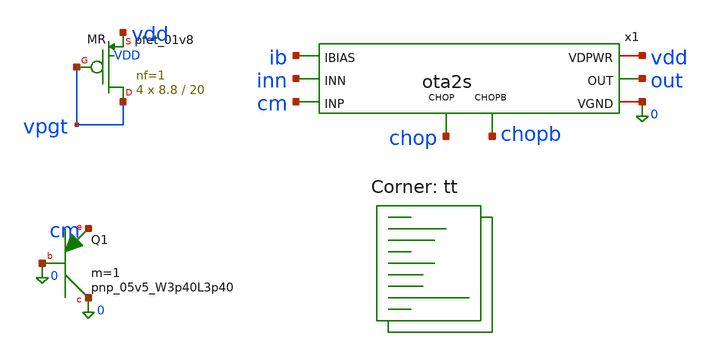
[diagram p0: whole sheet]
** sch_path: xschem/tb_m3_sens.sch
**.subckt tb_m3_sens
x1 cm inn out vdd 0 ib chop chopb ota2s
XMR vpgt vpgt vdd VDD sky130_fd_pr__pfet_01v8 L=20 W=8.8 nf=1 ad='int((1 + 1)/2) * 8.8 / 1 * 0.29' as='int((1 + 2)/2) * 8.8 / 1 * 0.29'
+ pd='2*int((1 + 1)/2) * (8.8 / 1 + 0.29)' ps='2*int((1 + 2)/2) * (8.8 / 1 + 0.29)' nrd='0.29 / 8.8 ' nrs='0.29 / 8.8 '
+ sa=0 sb=0 sd=0 mult=4 m=4
XQ1 0 0 cm sky130_fd_pr__pnp_05v5_W3p40L3p40 m=1
**** begin user architecture code
.lib $::SKYWATER_MODELS/sky130.lib.spice tt

.param vdd=1.8 rs=1
.temp 25
Vdd vdd 0 {vdd}
* door 1: input CM = a real diode PNP carrying I_PTAT(T)
* rs = R1 corner (1 nominal, 1.17 ll, 0.88 hh); the denominator is R1's own tempco
Bcm vdd cm I = 2.79e-6*rs*(temper+273.15)/298.15/(1+4.89e-4*(temper-27)+1.2e-6*(temper-27)**2)
* door 2: PTAT bias, I_PTAT/2, sunk from IBIAS
Bib ib 0 I = 1.40e-6*rs*(temper+273.15)/298.15/(1+4.89e-4*(temper-27)+1.2e-6*(temper-27)**2)
* door 4: replica P1 carries I_PTAT -> its gate is the vpg target
Brp vpgt 0 I = 2.79e-6*rs*(temper+273.15)/298.15/(1+4.89e-4*(temper-27)+1.2e-6*(temper-27)**2)
* chop state A (swap the two values for state B)
Vchop chop 0 0
Vchopb chopb 0 {vdd}
* servo: plays the bandgap loop, moves INN until out = vpgt
Bsv inn cm V = 0.5*tanh(2000*(v(out)-v(vpgt)))
.control
option reltol=1e-5 vntol=1e-9
option temp=25
let s = vector(9)
op
let s[0] = (v(cm)-v(inn))*1e6
alter @m.x1.xmp1.msky130_fd_pr__pfet_01v8_lvt[delvto] = 1e-3
op
let s[1] = ((v(cm)-v(inn))*1e6 - s[0])/1000
alter @m.x1.xmp1.msky130_fd_pr__pfet_01v8_lvt[delvto] = 0
alter @m.x1.xmp2.msky130_fd_pr__pfet_01v8_lvt[delvto] = 1e-3
op
let s[2] = ((v(cm)-v(inn))*1e6 - s[0])/1000
alter @m.x1.xmp2.msky130_fd_pr__pfet_01v8_lvt[delvto] = 0
alter @m.x1.xmn1.msky130_fd_pr__nfet_01v8[delvto] = 1e-3
op
let s[3] = ((v(cm)-v(inn))*1e6 - s[0])/1000
alter @m.x1.xmn1.msky130_fd_pr__nfet_01v8[delvto] = 0
alter @m.x1.xmn2.msky130_fd_pr__nfet_01v8[delvto] = 1e-3
op
let s[4] = ((v(cm)-v(inn))*1e6 - s[0])/1000
alter @m.x1.xmn2.msky130_fd_pr__nfet_01v8[delvto] = 0
alter @m.x1.xmn3.msky130_fd_pr__nfet_01v8[delvto] = 1e-3
op
let s[5] = ((v(cm)-v(inn))*1e6 - s[0])/1000
alter @m.x1.xmn3.msky130_fd_pr__nfet_01v8[delvto] = 0
alter @m.x1.xmtail.msky130_fd_pr__pfet_01v8[delvto] = 1e-3
op
let s[6] = ((v(cm)-v(inn))*1e6 - s[0])/1000
alter @m.x1.xmtail.msky130_fd_pr__pfet_01v8[delvto] = 0
alter @m.x1.xmp3.msky130_fd_pr__pfet_01v8[delvto] = 1e-3
op
let s[7] = ((v(cm)-v(inn))*1e6 - s[0])/1000
alter @m.x1.xmp3.msky130_fd_pr__pfet_01v8[delvto] = 0
alter @m.x1.xmref.msky130_fd_pr__pfet_01v8[delvto] = 1e-3
op
let s[8] = ((v(cm)-v(inn))*1e6 - s[0])/1000
alter @m.x1.xmref.msky130_fd_pr__pfet_01v8[delvto] = 0
let vos0 = s[0]
let smp1 = s[1]
let smp2 = s[2]
let smn1 = s[3]
let smn2 = s[4]
let smn3 = s[5]
let smtail = s[6]
let smp3 = s[7]
let smref = s[8]
echo SENS vos0_uV=$&vos0 mp1=$&smp1 mp2=$&smp2 mn1=$&smn1 mn2=$&smn2 mn3=$&smn3 mtail=$&smtail mp3=$&smp3 mref=$&smref
.endc
.endc

**** end user architecture code
**.ends

* expanding   symbol:  ota2s.sym # of pins=8
** sym_path: xschem/ota2s.sym
** sch_path: xschem/ota2s.sch
.subckt ota2s INP INN OUT VDPWR VGND IBIAS CHOP CHOPB
*.ipin INN
*.ipin INP
*.ipin IBIAS
*.opin OUT
*.iopin VDPWR
*.iopin VGND
*.ipin CHOPB
*.ipin CHOP
XMREF IBIAS IBIAS VDPWR VDPWR sky130_fd_pr__pfet_01v8 L=4 W=20 nf=1 ad='int((1 + 1)/2) * 20 / 1 * 0.29' as='int((1
+ + 2)/2) * 20 / 1 * 0.29' pd='2*int((1 + 1)/2) * (20 / 1 + 0.29)' ps='2*int((1 + 2)/2) * (20 / 1 + 0.29)' nrd='0.29
+ / 20 ' nrs='0.29 / 20 ' sa=0 sb=0 sd=0 mult=1 m=1
XMTAIL tail IBIAS VDPWR VDPWR sky130_fd_pr__pfet_01v8 L=4 W=20 nf=1 ad='int((1 + 1)/2) * 20 / 1 * 0.29' as='int((1
+ + 2)/2) * 20 / 1 * 0.29' pd='2*int((1 + 1)/2) * (20 / 1 + 0.29)' ps='2*int((1 + 2)/2) * (20 / 1 + 0.29)' nrd='0.29
+ / 20 ' nrs='0.29 / 20 ' sa=0 sb=0 sd=0 mult=2 m=2
XMP1 d1 INN tail VDPWR sky130_fd_pr__pfet_01v8_lvt L=6 W=25 nf=1 ad='int((1 + 1)/2) * 25 / 1 * 0.29' as='int((1
+ + 2)/2) * 25 / 1 * 0.29' pd='2*int((1 + 1)/2) * (25 / 1 + 0.29)' ps='2*int((1 + 2)/2) * (25 / 1 + 0.29)' nrd='0.29
+ / 25 ' nrs='0.29 / 25 ' sa=0 sb=0 sd=0 mult=24 m=24
XMP2 x1 INP tail VDPWR sky130_fd_pr__pfet_01v8_lvt L=6 W=25 nf=1 ad='int((1 + 1)/2) * 25 / 1 * 0.29' as='int((1
+ + 2)/2) * 25 / 1 * 0.29' pd='2*int((1 + 1)/2) * (25 / 1 + 0.29)' ps='2*int((1 + 2)/2) * (25 / 1 + 0.29)' nrd='0.29
+ / 25 ' nrs='0.29 / 25 ' sa=0 sb=0 sd=0 mult=24 m=24
XMN1 d1 g12 VGND VGND sky130_fd_pr__nfet_01v8 L=20 W=6 nf=1 ad='int((1 + 1)/2) * 6 / 1 * 0.29' as='int((1
+ + 2)/2) * 6 / 1 * 0.29' pd='2*int((1 + 1)/2) * (6 / 1 + 0.29)' ps='2*int((1 + 2)/2) * (6 / 1 + 0.29)' nrd='0.29
+ / 6 ' nrs='0.29 / 6 ' sa=0 sb=0 sd=0 mult=2 m=2
XMN2 x1 g12 VGND VGND sky130_fd_pr__nfet_01v8 L=20 W=6 nf=1 ad='int((1 + 1)/2) * 6 / 1 * 0.29' as='int((1
+ + 2)/2) * 6 / 1 * 0.29' pd='2*int((1 + 1)/2) * (6 / 1 + 0.29)' ps='2*int((1 + 2)/2) * (6 / 1 + 0.29)' nrd='0.29
+ / 6 ' nrs='0.29 / 6 ' sa=0 sb=0 sd=0 mult=2 m=2
XMP3 OUT IBIAS VDPWR VDPWR sky130_fd_pr__pfet_01v8 L=4 W=20 nf=1 ad='int((1 + 1)/2) * 20 / 1 * 0.29' as='int((1
+ + 2)/2) * 20 / 1 * 0.29' pd='2*int((1 + 1)/2) * (20 / 1 + 0.29)' ps='2*int((1 + 2)/2) * (20 / 1 + 0.29)' nrd='0.29
+ / 20 ' nrs='0.29 / 20 ' sa=0 sb=0 sd=0 mult=6 m=6
XMN3 OUT g3 VGND VGND sky130_fd_pr__nfet_01v8 L=1 W=7 nf=1 ad='int((1 + 1)/2) * 7 / 1 * 0.29' as='int((1
+ + 2)/2) * 7 / 1 * 0.29' pd='2*int((1 + 1)/2) * (7 / 1 + 0.29)' ps='2*int((1 + 2)/2) * (7 / 1 + 0.29)' nrd='0.29
+ / 7 ' nrs='0.29 / 7 ' sa=0 sb=0 sd=0 mult=1 m=1
XRZ1 net1 g3 VGND sky130_fd_pr__res_high_po_1p41 L=20 mult=1 m=1
XRZ2 net2 net1 VGND sky130_fd_pr__res_high_po_1p41 L=20 mult=1 m=1
XRZ3 net3 net2 VGND sky130_fd_pr__res_high_po_1p41 L=20 mult=1 m=1
XRZ4 net4 net3 VGND sky130_fd_pr__res_high_po_1p41 L=20 mult=1 m=1
XRZ5 net5 net4 VGND sky130_fd_pr__res_high_po_1p41 L=20 mult=1 m=1
XRZ6 cz net5 VGND sky130_fd_pr__res_high_po_1p41 L=20 mult=1 m=1
XCC cz OUT sky130_fd_pr__cap_mim_m3_1 W=25 L=25 MF=8 m=8
XDP tail VDPWR tail VDPWR sky130_fd_pr__pfet_01v8_lvt L=6 W=25 nf=1 ad='int((1 + 1)/2) * 25 / 1 * 0.29' as='int((1
+ + 2)/2) * 25 / 1 * 0.29' pd='2*int((1 + 1)/2) * (25 / 1 + 0.29)' ps='2*int((1 + 2)/2) * (25 / 1 + 0.29)' nrd='0.29
+ / 25 ' nrs='0.29 / 25 ' sa=0 sb=0 sd=0 mult=8 m=8
XDNA d1 VGND VGND VGND sky130_fd_pr__nfet_01v8 L=20 W=6 nf=1 ad='int((1 + 1)/2) * 6 / 1 * 0.29' as='int((1
+ + 2)/2) * 6 / 1 * 0.29' pd='2*int((1 + 1)/2) * (6 / 1 + 0.29)' ps='2*int((1 + 2)/2) * (6 / 1 + 0.29)' nrd='0.29
+ / 6 ' nrs='0.29 / 6 ' sa=0 sb=0 sd=0 mult=2 m=2
XDNB x1 VGND VGND VGND sky130_fd_pr__nfet_01v8 L=20 W=6 nf=1 ad='int((1 + 1)/2) * 6 / 1 * 0.29' as='int((1
+ + 2)/2) * 6 / 1 * 0.29' pd='2*int((1 + 1)/2) * (6 / 1 + 0.29)' ps='2*int((1 + 2)/2) * (6 / 1 + 0.29)' nrd='0.29
+ / 6 ' nrs='0.29 / 6 ' sa=0 sb=0 sd=0 mult=2 m=2
XDB VDPWR VDPWR VDPWR VDPWR sky130_fd_pr__pfet_01v8 L=4 W=20 nf=1 ad='int((1 + 1)/2) * 20 / 1 * 0.29' as='int((1
+ + 2)/2) * 20 / 1 * 0.29' pd='2*int((1 + 1)/2) * (20 / 1 + 0.29)' ps='2*int((1 + 2)/2) * (20 / 1 + 0.29)' nrd='0.29
+ / 20 ' nrs='0.29 / 20 ' sa=0 sb=0 sd=0 mult=2 m=2
XRD1 VGND VGND VGND sky130_fd_pr__res_high_po_1p41 L=20 mult=1 m=1
XRD2 VGND VGND VGND sky130_fd_pr__res_high_po_1p41 L=20 mult=1 m=1
XSD1 d1 CHOPB g12 VGND sky130_fd_pr__nfet_01v8 L=0.5 W=6 nf=1 ad='int((1 + 1)/2) * 6 / 1 * 0.29' as='int((1
+ + 2)/2) * 6 / 1 * 0.29' pd='2*int((1 + 1)/2) * (6 / 1 + 0.29)' ps='2*int((1 + 2)/2) * (6 / 1 + 0.29)' nrd='0.29
+ / 6 ' nrs='0.29 / 6 ' sa=0 sb=0 sd=0 mult=1 m=1
XSD2 x1 CHOP g12 VGND sky130_fd_pr__nfet_01v8 L=0.5 W=6 nf=1 ad='int((1 + 1)/2) * 6 / 1 * 0.29' as='int((1
+ + 2)/2) * 6 / 1 * 0.29' pd='2*int((1 + 1)/2) * (6 / 1 + 0.29)' ps='2*int((1 + 2)/2) * (6 / 1 + 0.29)' nrd='0.29
+ / 6 ' nrs='0.29 / 6 ' sa=0 sb=0 sd=0 mult=1 m=1
XSG2 g3 CHOP d1 VGND sky130_fd_pr__nfet_01v8 L=0.5 W=6 nf=1 ad='int((1 + 1)/2) * 6 / 1 * 0.29' as='int((1
+ + 2)/2) * 6 / 1 * 0.29' pd='2*int((1 + 1)/2) * (6 / 1 + 0.29)' ps='2*int((1 + 2)/2) * (6 / 1 + 0.29)' nrd='0.29
+ / 6 ' nrs='0.29 / 6 ' sa=0 sb=0 sd=0 mult=1 m=1
XSG1 x1 CHOPB g3 VGND sky130_fd_pr__nfet_01v8 L=0.5 W=6 nf=1 ad='int((1 + 1)/2) * 6 / 1 * 0.29' as='int((1
+ + 2)/2) * 6 / 1 * 0.29' pd='2*int((1 + 1)/2) * (6 / 1 + 0.29)' ps='2*int((1 + 2)/2) * (6 / 1 + 0.29)' nrd='0.29
+ / 6 ' nrs='0.29 / 6 ' sa=0 sb=0 sd=0 mult=1 m=1
.ends

.end
